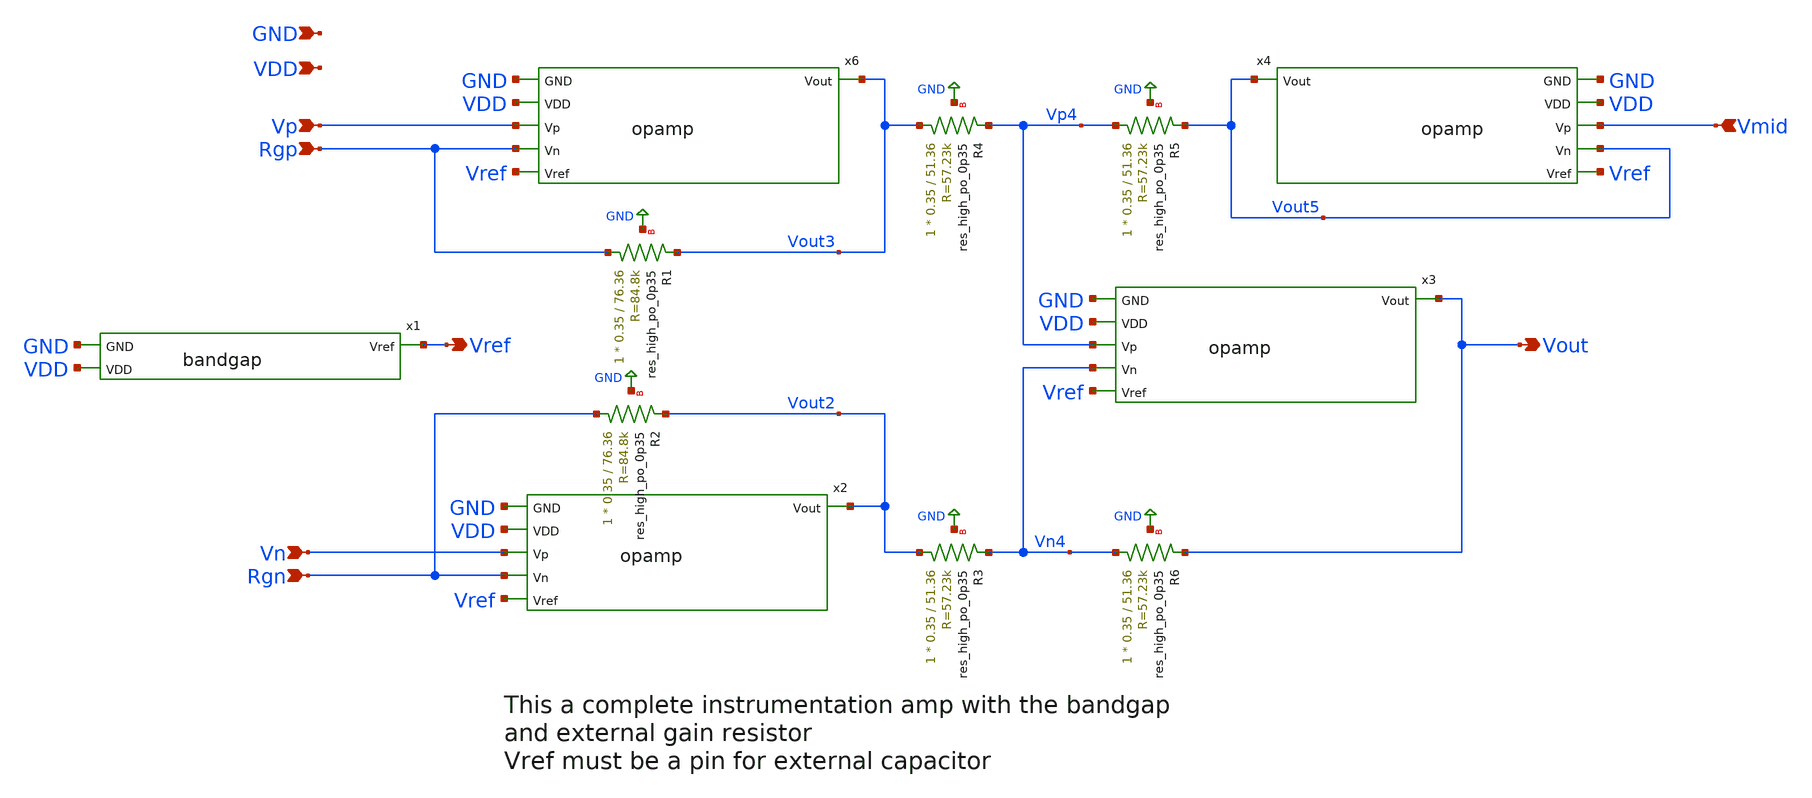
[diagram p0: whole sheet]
** sch_path: xschem/instamp.sch
* Copyright 2021 Stefan Frederik Schippers
* Licensed under the Apache License, Version 2.0 (the "License");
* you may not use this file except in compliance with the License.
* You may obtain a copy of the License at
* https://www.apache.org/licenses/LICENSE-2.0
* Unless required by applicable law or agreed to in writing, software
* distributed under the License is distributed on an "AS IS" BASIS,
* WITHOUT WARRANTIES OR CONDITIONS OF ANY KIND, either express or implied.
* See the License for the specific language governing permissions and
* limitations under the License.
**.subckt instamp Vp Vn Vout Vref Rgp Rgn Vmid GND VDD
*.ipin Vp
*.ipin Vn
*.opin Vout
*.opin Vref
*.ipin Rgp
*.ipin Rgn
*.ipin Vmid
*.ipin GND
*.ipin VDD
XR1 Rgp Vout3 GND sky130_fd_pr__res_high_po_0p35 L=76.36 mult=1 m=1
XR2 Rgn Vout2 GND sky130_fd_pr__res_high_po_0p35 L=76.36 mult=1 m=1
XR3 Vout2 Vn4 GND sky130_fd_pr__res_high_po_0p35 L=51.36 mult=1 m=1
XR4 Vout3 Vp4 GND sky130_fd_pr__res_high_po_0p35 L=51.36 mult=1 m=1
XR5 Vp4 Vout5 GND sky130_fd_pr__res_high_po_0p35 L=51.36 mult=1 m=1
XR6 Vn4 Vout GND sky130_fd_pr__res_high_po_0p35 L=51.36 mult=1 m=1
x6 Vref Vout3 Vp Rgp VDD GND opamp
x2 Vref Vout2 Vn Rgn VDD GND opamp
x3 Vref Vout Vp4 Vn4 VDD GND opamp
x4 Vref Vout5 Vmid Vout5 VDD GND opamp
x1 Vref GND VDD bandgap
**.ends

* expanding   symbol:  opamp.sym # of pins=6
** sym_path: xschem/opamp.sym
** sch_path: xschem/opamp.sch
.subckt opamp Vref Vout Vp Vn VDD GND
*.opin Vout
*.ipin Vref
*.ipin Vp
*.ipin Vn
*.ipin GND
*.ipin VDD
XM1 Vg1 Vg1 net1 GND sky130_fd_pr__nfet_g5v0d10v5 L=2 W=3.33 nf=1 ad='int((1 + 1)/2) * 3.33 / 1 * 0.29'
+ as='int((1 + 2)/2) * 3.33 / 1 * 0.29' pd='2*int((1 + 1)/2) * (3.33 / 1 + 0.29)' ps='2*int((1 + 2)/2) * (3.33 / 1 + 0.29)'
+ nrd='0.29 / 3.33 ' nrs='0.29 / 3.33 ' sa=0 sb=0 sd=0 mult=3 m=3
XM2 net1 Vg1 GND GND sky130_fd_pr__nfet_g5v0d10v5 L=5 W=5 nf=1 ad='int((1 + 1)/2) * 5 / 1 * 0.29' as='int((1 + 2)/2) * 5 / 1 * 0.29'
+ pd='2*int((1 + 1)/2) * (5 / 1 + 0.29)' ps='2*int((1 + 2)/2) * (5 / 1 + 0.29)' nrd='0.29 / 5 ' nrs='0.29 / 5 '
+ sa=0 sb=0 sd=0 mult=1 m=1
XM4 net2 Vg1 GND GND sky130_fd_pr__nfet_g5v0d10v5 L=5 W=5 nf=1 ad='int((1 + 1)/2) * 5 / 1 * 0.29' as='int((1 + 2)/2) * 5 / 1 * 0.29'
+ pd='2*int((1 + 1)/2) * (5 / 1 + 0.29)' ps='2*int((1 + 2)/2) * (5 / 1 + 0.29)' nrd='0.29 / 5 ' nrs='0.29 / 5 '
+ sa=0 sb=0 sd=0 mult=1 m=1
XM3 Vg5 Vg1 net2 GND sky130_fd_pr__nfet_g5v0d10v5 L=2 W=3.33 nf=1 ad='int((1 + 1)/2) * 3.33 / 1 * 0.29'
+ as='int((1 + 2)/2) * 3.33 / 1 * 0.29' pd='2*int((1 + 1)/2) * (3.33 / 1 + 0.29)' ps='2*int((1 + 2)/2) * (3.33 / 1 + 0.29)'
+ nrd='0.29 / 3.33 ' nrs='0.29 / 3.33 ' sa=0 sb=0 sd=0 mult=3 m=3
XMr1 net6 Vref GND GND sky130_fd_pr__nfet_g5v0d10v5 L=8 W=5 nf=1 ad='int((1 + 1)/2) * 5 / 1 * 0.29' as='int((1 + 2)/2) * 5 / 1 * 0.29'
+ pd='2*int((1 + 1)/2) * (5 / 1 + 0.29)' ps='2*int((1 + 2)/2) * (5 / 1 + 0.29)' nrd='0.29 / 5 ' nrs='0.29 / 5 '
+ sa=0 sb=0 sd=0 mult=1 m=1
XMr2 VgR2 VgR2 VDD VDD sky130_fd_pr__pfet_g5v0d10v5 L=5 W=4 nf=1 ad='int((1 + 1)/2) * 4 / 1 * 0.29' as='int((1 + 2)/2) * 4 / 1 * 0.29'
+ pd='2*int((1 + 1)/2) * (4 / 1 + 0.29)' ps='2*int((1 + 2)/2) * (4 / 1 + 0.29)' nrd='0.29 / 4 ' nrs='0.29 / 4 '
+ sa=0 sb=0 sd=0 mult=1 m=1
XMr3 Vg1 VgR2 VDD VDD sky130_fd_pr__pfet_g5v0d10v5 L=5 W=4 nf=1 ad='int((1 + 1)/2) * 4 / 1 * 0.29' as='int((1 + 2)/2) * 4 / 1 * 0.29'
+ pd='2*int((1 + 1)/2) * (4 / 1 + 0.29)' ps='2*int((1 + 2)/2) * (4 / 1 + 0.29)' nrd='0.29 / 4 ' nrs='0.29 / 4 '
+ sa=0 sb=0 sd=0 mult=1 m=1
XM32 net3 Vg1 GND GND sky130_fd_pr__nfet_g5v0d10v5 L=5 W=10 nf=1 ad='int((1 + 1)/2) * 10 / 1 * 0.29'
+ as='int((1 + 2)/2) * 10 / 1 * 0.29' pd='2*int((1 + 1)/2) * (10 / 1 + 0.29)' ps='2*int((1 + 2)/2) * (10 / 1 + 0.29)'
+ nrd='0.29 / 10 ' nrs='0.29 / 10 ' sa=0 sb=0 sd=0 mult=1 m=1
XM31 Vs29 Vg1 net3 GND sky130_fd_pr__nfet_g5v0d10v5 L=2 W=6.66 nf=1 ad='int((1 + 1)/2) * 6.66 / 1 * 0.29'
+ as='int((1 + 2)/2) * 6.66 / 1 * 0.29' pd='2*int((1 + 1)/2) * (6.66 / 1 + 0.29)' ps='2*int((1 + 2)/2) * (6.66 / 1 + 0.29)'
+ nrd='0.29 / 6.66 ' nrs='0.29 / 6.66 ' sa=0 sb=0 sd=0 mult=3 m=3
XM15 Vg11 Vg1 Vd10 GND sky130_fd_pr__nfet_g5v0d10v5 L=2 W=14.3 nf=1 ad='int((1 + 1)/2) * 14.3 / 1 * 0.29'
+ as='int((1 + 2)/2) * 14.3 / 1 * 0.29' pd='2*int((1 + 1)/2) * (14.3 / 1 + 0.29)' ps='2*int((1 + 2)/2) * (14.3 / 1 + 0.29)'
+ nrd='0.29 / 14.3 ' nrs='0.29 / 14.3 ' sa=0 sb=0 sd=0 mult=7 m=7
XM16 Vd10 Vg1 GND GND sky130_fd_pr__nfet_g5v0d10v5 L=5 W=10 nf=1 ad='int((1 + 1)/2) * 10 / 1 * 0.29'
+ as='int((1 + 2)/2) * 10 / 1 * 0.29' pd='2*int((1 + 1)/2) * (10 / 1 + 0.29)' ps='2*int((1 + 2)/2) * (10 / 1 + 0.29)'
+ nrd='0.29 / 10 ' nrs='0.29 / 10 ' sa=0 sb=0 sd=0 mult=1 m=1
XM18 Vd9 Vg1 GND GND sky130_fd_pr__nfet_g5v0d10v5 L=5 W=10 nf=1 ad='int((1 + 1)/2) * 10 / 1 * 0.29' as='int((1 + 2)/2) * 10 / 1 * 0.29'
+ pd='2*int((1 + 1)/2) * (10 / 1 + 0.29)' ps='2*int((1 + 2)/2) * (10 / 1 + 0.29)' nrd='0.29 / 10 ' nrs='0.29 / 10 '
+ sa=0 sb=0 sd=0 mult=1 m=1
XM17 Vg28 Vg1 Vd9 GND sky130_fd_pr__nfet_g5v0d10v5 L=2 W=14.3 nf=1 ad='int((1 + 1)/2) * 14.3 / 1 * 0.29'
+ as='int((1 + 2)/2) * 14.3 / 1 * 0.29' pd='2*int((1 + 1)/2) * (14.3 / 1 + 0.29)' ps='2*int((1 + 2)/2) * (14.3 / 1 + 0.29)'
+ nrd='0.29 / 14.3 ' nrs='0.29 / 14.3 ' sa=0 sb=0 sd=0 mult=7 m=7
XM20 Vg22 Vg1 GND GND sky130_fd_pr__nfet_g5v0d10v5 L=5 W=1.5 nf=1 ad='int((1 + 1)/2) * 1.5 / 1 * 0.29'
+ as='int((1 + 2)/2) * 1.5 / 1 * 0.29' pd='2*int((1 + 1)/2) * (1.5 / 1 + 0.29)' ps='2*int((1 + 2)/2) * (1.5 / 1 + 0.29)'
+ nrd='0.29 / 1.5 ' nrs='0.29 / 1.5 ' sa=0 sb=0 sd=0 mult=1 m=1
XM26 Vg26 Vg26 GND GND sky130_fd_pr__nfet_g5v0d10v5 L=0.5 W=5 nf=1 ad='int((1 + 1)/2) * 5 / 1 * 0.29'
+ as='int((1 + 2)/2) * 5 / 1 * 0.29' pd='2*int((1 + 1)/2) * (5 / 1 + 0.29)' ps='2*int((1 + 2)/2) * (5 / 1 + 0.29)'
+ nrd='0.29 / 5 ' nrs='0.29 / 5 ' sa=0 sb=0 sd=0 mult=5 m=5
XM25 Vd24 Vd24 Vg26 GND sky130_fd_pr__nfet_g5v0d10v5 L=0.5 W=5 nf=1 ad='int((1 + 1)/2) * 5 / 1 * 0.29'
+ as='int((1 + 2)/2) * 5 / 1 * 0.29' pd='2*int((1 + 1)/2) * (5 / 1 + 0.29)' ps='2*int((1 + 2)/2) * (5 / 1 + 0.29)'
+ nrd='0.29 / 5 ' nrs='0.29 / 5 ' sa=0 sb=0 sd=0 mult=5 m=5
XM23 Vg27 Vd24 Vg28 GND sky130_fd_pr__nfet_g5v0d10v5 L=0.5 W=10 nf=1 ad='int((1 + 1)/2) * 10 / 1 * 0.29'
+ as='int((1 + 2)/2) * 10 / 1 * 0.29' pd='2*int((1 + 1)/2) * (10 / 1 + 0.29)' ps='2*int((1 + 2)/2) * (10 / 1 + 0.29)'
+ nrd='0.29 / 10 ' nrs='0.29 / 10 ' sa=0 sb=0 sd=0 mult=5 m=5
XM28 Vout Vg28 GND GND sky130_fd_pr__nfet_g5v0d10v5 L=0.5 W=10 nf=1 ad='int((1 + 1)/2) * 10 / 1 * 0.29'
+ as='int((1 + 2)/2) * 10 / 1 * 0.29' pd='2*int((1 + 1)/2) * (10 / 1 + 0.29)' ps='2*int((1 + 2)/2) * (10 / 1 + 0.29)'
+ nrd='0.29 / 10 ' nrs='0.29 / 10 ' sa=0 sb=0 sd=0 mult=15 m=15
XM30 Vd30 Vn Vs29 GND sky130_fd_pr__nfet_g5v0d10v5 L=1.5 W=11.11 nf=1 ad='int((1 + 1)/2) * 11.11 / 1 * 0.29'
+ as='int((1 + 2)/2) * 11.11 / 1 * 0.29' pd='2*int((1 + 1)/2) * (11.11 / 1 + 0.29)' ps='2*int((1 + 2)/2) * (11.11 / 1 + 0.29)'
+ nrd='0.29 / 11.11 ' nrs='0.29 / 11.11 ' sa=0 sb=0 sd=0 mult=9 m=9
XM29 Vd29 Vp Vs29 GND sky130_fd_pr__nfet_g5v0d10v5 L=1.5 W=11.11 nf=1 ad='int((1 + 1)/2) * 11.11 / 1 * 0.29'
+ as='int((1 + 2)/2) * 11.11 / 1 * 0.29' pd='2*int((1 + 1)/2) * (11.11 / 1 + 0.29)' ps='2*int((1 + 2)/2) * (11.11 / 1 + 0.29)'
+ nrd='0.29 / 11.11 ' nrs='0.29 / 11.11 ' sa=0 sb=0 sd=0 mult=9 m=9
XM5 net4 Vg5 VDD VDD sky130_fd_pr__pfet_g5v0d10v5 L=5 W=5 nf=1 ad='int((1 + 1)/2) * 5 / 1 * 0.29' as='int((1 + 2)/2) * 5 / 1 * 0.29'
+ pd='2*int((1 + 1)/2) * (5 / 1 + 0.29)' ps='2*int((1 + 2)/2) * (5 / 1 + 0.29)' nrd='0.29 / 5 ' nrs='0.29 / 5 '
+ sa=0 sb=0 sd=0 mult=3 m=3
XM6 Vg5 Vg5 net4 VDD sky130_fd_pr__pfet_g5v0d10v5 L=2 W=6.6 nf=1 ad='int((1 + 1)/2) * 6.6 / 1 * 0.29'
+ as='int((1 + 2)/2) * 6.6 / 1 * 0.29' pd='2*int((1 + 1)/2) * (6.6 / 1 + 0.29)' ps='2*int((1 + 2)/2) * (6.6 / 1 + 0.29)'
+ nrd='0.29 / 6.6 ' nrs='0.29 / 6.6 ' sa=0 sb=0 sd=0 mult=3 m=3
XM7 net5 Vg5 VDD VDD sky130_fd_pr__pfet_g5v0d10v5 L=5 W=10 nf=1 ad='int((1 + 1)/2) * 10 / 1 * 0.29' as='int((1 + 2)/2) * 10 / 1 * 0.29'
+ pd='2*int((1 + 1)/2) * (10 / 1 + 0.29)' ps='2*int((1 + 2)/2) * (10 / 1 + 0.29)' nrd='0.29 / 10 ' nrs='0.29 / 10 '
+ sa=0 sb=0 sd=0 mult=3 m=3
XM8 Vd8 Vg5 net5 VDD sky130_fd_pr__pfet_g5v0d10v5 L=2 W=13.2 nf=1 ad='int((1 + 1)/2) * 13.2 / 1 * 0.29'
+ as='int((1 + 2)/2) * 13.2 / 1 * 0.29' pd='2*int((1 + 1)/2) * (13.2 / 1 + 0.29)' ps='2*int((1 + 2)/2) * (13.2 / 1 + 0.29)'
+ nrd='0.29 / 13.2 ' nrs='0.29 / 13.2 ' sa=0 sb=0 sd=0 mult=3 m=3
XM09 Vd9 Vp Vd8 Vd8 sky130_fd_pr__pfet_g5v0d10v5 L=1.5 W=22.22 nf=1 ad='int((1 + 1)/2) * 22.22 / 1 * 0.29'
+ as='int((1 + 2)/2) * 22.22 / 1 * 0.29' pd='2*int((1 + 1)/2) * (22.22 / 1 + 0.29)' ps='2*int((1 + 2)/2) * (22.22 / 1 + 0.29)'
+ nrd='0.29 / 22.22 ' nrs='0.29 / 22.22 ' sa=0 sb=0 sd=0 mult=9 m=9
XM010 Vd10 Vn Vd8 Vd8 sky130_fd_pr__pfet_g5v0d10v5 L=1.5 W=22.22 nf=1 ad='int((1 + 1)/2) * 22.22 / 1 * 0.29'
+ as='int((1 + 2)/2) * 22.22 / 1 * 0.29' pd='2*int((1 + 1)/2) * (22.22 / 1 + 0.29)' ps='2*int((1 + 2)/2) * (22.22 / 1 + 0.29)'
+ nrd='0.29 / 22.22 ' nrs='0.29 / 22.22 ' sa=0 sb=0 sd=0 mult=9 m=9
XM13 Vd29 Vg11 VDD VDD sky130_fd_pr__pfet_g5v0d10v5 L=2.5 W=10 nf=1 ad='int((1 + 1)/2) * 10 / 1 * 0.29'
+ as='int((1 + 2)/2) * 10 / 1 * 0.29' pd='2*int((1 + 1)/2) * (10 / 1 + 0.29)' ps='2*int((1 + 2)/2) * (10 / 1 + 0.29)'
+ nrd='0.29 / 10 ' nrs='0.29 / 10 ' sa=0 sb=0 sd=0 mult=5 m=5
XM14 Vg27 Vg11 Vd29 VDD sky130_fd_pr__pfet_g5v0d10v5 L=1 W=10 nf=1 ad='int((1 + 1)/2) * 10 / 1 * 0.29'
+ as='int((1 + 2)/2) * 10 / 1 * 0.29' pd='2*int((1 + 1)/2) * (10 / 1 + 0.29)' ps='2*int((1 + 2)/2) * (10 / 1 + 0.29)'
+ nrd='0.29 / 10 ' nrs='0.29 / 10 ' sa=0 sb=0 sd=0 mult=5 m=5
XM11 Vd30 Vg11 VDD VDD sky130_fd_pr__pfet_g5v0d10v5 L=2.5 W=10 nf=1 ad='int((1 + 1)/2) * 10 / 1 * 0.29'
+ as='int((1 + 2)/2) * 10 / 1 * 0.29' pd='2*int((1 + 1)/2) * (10 / 1 + 0.29)' ps='2*int((1 + 2)/2) * (10 / 1 + 0.29)'
+ nrd='0.29 / 10 ' nrs='0.29 / 10 ' sa=0 sb=0 sd=0 mult=5 m=5
XM12 Vg11 Vg11 Vd30 VDD sky130_fd_pr__pfet_g5v0d10v5 L=1 W=10 nf=1 ad='int((1 + 1)/2) * 10 / 1 * 0.29'
+ as='int((1 + 2)/2) * 10 / 1 * 0.29' pd='2*int((1 + 1)/2) * (10 / 1 + 0.29)' ps='2*int((1 + 2)/2) * (10 / 1 + 0.29)'
+ nrd='0.29 / 10 ' nrs='0.29 / 10 ' sa=0 sb=0 sd=0 mult=5 m=5
XM021 Vg21 Vg21 VDD VDD sky130_fd_pr__pfet_g5v0d10v5 L=0.5 W=15 nf=1 ad='int((1 + 1)/2) * 15 / 1 * 0.29'
+ as='int((1 + 2)/2) * 15 / 1 * 0.29' pd='2*int((1 + 1)/2) * (15 / 1 + 0.29)' ps='2*int((1 + 2)/2) * (15 / 1 + 0.29)'
+ nrd='0.29 / 15 ' nrs='0.29 / 15 ' sa=0 sb=0 sd=0 mult=5 m=5
XM022 Vg22 Vg22 Vg21 VDD sky130_fd_pr__pfet_g5v0d10v5 L=0.5 W=15 nf=1 ad='int((1 + 1)/2) * 15 / 1 * 0.29'
+ as='int((1 + 2)/2) * 15 / 1 * 0.29' pd='2*int((1 + 1)/2) * (15 / 1 + 0.29)' ps='2*int((1 + 2)/2) * (15 / 1 + 0.29)'
+ nrd='0.29 / 15 ' nrs='0.29 / 15 ' sa=0 sb=0 sd=0 mult=5 m=5
XM24 Vd24 Vg5 VDD VDD sky130_fd_pr__pfet_g5v0d10v5 L=5 W=4 nf=1 ad='int((1 + 1)/2) * 4 / 1 * 0.29' as='int((1 + 2)/2) * 4 / 1 * 0.29'
+ pd='2*int((1 + 1)/2) * (4 / 1 + 0.29)' ps='2*int((1 + 2)/2) * (4 / 1 + 0.29)' nrd='0.29 / 4 ' nrs='0.29 / 4 '
+ sa=0 sb=0 sd=0 mult=1 m=1
XM27 Vout Vg27 VDD VDD sky130_fd_pr__pfet_g5v0d10v5 L=0.5 W=15 nf=1 ad='int((1 + 1)/2) * 15 / 1 * 0.29'
+ as='int((1 + 2)/2) * 15 / 1 * 0.29' pd='2*int((1 + 1)/2) * (15 / 1 + 0.29)' ps='2*int((1 + 2)/2) * (15 / 1 + 0.29)'
+ nrd='0.29 / 15 ' nrs='0.29 / 15 ' sa=0 sb=0 sd=0 mult=25 m=25
XM19 Vg28 Vg22 Vg27 VDD sky130_fd_pr__pfet_g5v0d10v5 L=0.5 W=10 nf=1 ad='int((1 + 1)/2) * 10 / 1 * 0.29'
+ as='int((1 + 2)/2) * 10 / 1 * 0.29' pd='2*int((1 + 1)/2) * (10 / 1 + 0.29)' ps='2*int((1 + 2)/2) * (10 / 1 + 0.29)'
+ nrd='0.29 / 10 ' nrs='0.29 / 10 ' sa=0 sb=0 sd=0 mult=15 m=15
Vmeas_Iref VgR2 net6 0
.save i(vmeas_iref)
XC1 Vg27 Vout sky130_fd_pr__cap_mim_m3_1 W=30 L=20 MF=4 m=4
XC2 Vg28 Vout sky130_fd_pr__cap_mim_m3_1 W=30 L=20 MF=4 m=4
.ends


* expanding   symbol:  bandgap.sym # of pins=3
** sym_path: xschem/bandgap.sym
** sch_path: xschem/bandgap.sch
.subckt bandgap Vref GND VDD
*.opin Vref
*.ipin GND
*.ipin VDD
XM4 Vg3 Vg3 GND GND sky130_fd_pr__nfet_g5v0d10v5 L=1 W=20 nf=1 ad='int((1 + 1)/2) * 20 / 1 * 0.29' as='int((1 + 2)/2) * 20 / 1 * 0.29'
+ pd='2*int((1 + 1)/2) * (20 / 1 + 0.29)' ps='2*int((1 + 2)/2) * (20 / 1 + 0.29)' nrd='0.29 / 20 ' nrs='0.29 / 20 '
+ sa=0 sb=0 sd=0 mult=1 m=1
XQ1 GND GND Ve1 sky130_fd_pr__pnp_05v5_W3p40L3p40 m=24
XQ2 GND GND Vg2 sky130_fd_pr__pnp_05v5_W3p40L3p40 m=1
XM1 Vg10 Vg1 net1 net1 sky130_fd_pr__pfet_g5v0d10v5 L=1 W=20 nf=1 ad='int((1 + 1)/2) * 20 / 1 * 0.29'
+ as='int((1 + 2)/2) * 20 / 1 * 0.29' pd='2*int((1 + 1)/2) * (20 / 1 + 0.29)' ps='2*int((1 + 2)/2) * (20 / 1 + 0.29)'
+ nrd='0.29 / 20 ' nrs='0.29 / 20 ' sa=0 sb=0 sd=0 mult=1 m=1
XM2 Vg3 Vg2 net1 net1 sky130_fd_pr__pfet_g5v0d10v5 L=1 W=20 nf=1 ad='int((1 + 1)/2) * 20 / 1 * 0.29'
+ as='int((1 + 2)/2) * 20 / 1 * 0.29' pd='2*int((1 + 1)/2) * (20 / 1 + 0.29)' ps='2*int((1 + 2)/2) * (20 / 1 + 0.29)'
+ nrd='0.29 / 20 ' nrs='0.29 / 20 ' sa=0 sb=0 sd=0 mult=1 m=1
XM11 net1 Vg5 VDD VDD sky130_fd_pr__pfet_g5v0d10v5 L=1 W=1 nf=1 ad='int((1 + 1)/2) * 1 / 1 * 0.29' as='int((1 + 2)/2) * 1 / 1 * 0.29'
+ pd='2*int((1 + 1)/2) * (1 / 1 + 0.29)' ps='2*int((1 + 2)/2) * (1 / 1 + 0.29)' nrd='0.29 / 1 ' nrs='0.29 / 1 '
+ sa=0 sb=0 sd=0 mult=1 m=1
XM3 Vg10 Vg3 GND GND sky130_fd_pr__nfet_g5v0d10v5 L=1 W=20 nf=1 ad='int((1 + 1)/2) * 20 / 1 * 0.29' as='int((1 + 2)/2) * 20 / 1 * 0.29'
+ pd='2*int((1 + 1)/2) * (20 / 1 + 0.29)' ps='2*int((1 + 2)/2) * (20 / 1 + 0.29)' nrd='0.29 / 20 ' nrs='0.29 / 20 '
+ sa=0 sb=0 sd=0 mult=1 m=1
XM10 net2 Vg10 GND GND sky130_fd_pr__nfet_g5v0d10v5 L=1 W=20 nf=1 ad='int((1 + 1)/2) * 20 / 1 * 0.29'
+ as='int((1 + 2)/2) * 20 / 1 * 0.29' pd='2*int((1 + 1)/2) * (20 / 1 + 0.29)' ps='2*int((1 + 2)/2) * (20 / 1 + 0.29)'
+ nrd='0.29 / 20 ' nrs='0.29 / 20 ' sa=0 sb=0 sd=0 mult=1 m=1
XM8 Vg12 Vg5 VDD VDD sky130_fd_pr__pfet_g5v0d10v5 L=1 W=1 nf=1 ad='int((1 + 1)/2) * 1 / 1 * 0.29' as='int((1 + 2)/2) * 1 / 1 * 0.29'
+ pd='2*int((1 + 1)/2) * (1 / 1 + 0.29)' ps='2*int((1 + 2)/2) * (1 / 1 + 0.29)' nrd='0.29 / 1 ' nrs='0.29 / 1 '
+ sa=0 sb=0 sd=0 mult=1 m=1
XM5 Vg5 Vg5 VDD VDD sky130_fd_pr__pfet_g5v0d10v5 L=1 W=1 nf=1 ad='int((1 + 1)/2) * 1 / 1 * 0.29' as='int((1 + 2)/2) * 1 / 1 * 0.29'
+ pd='2*int((1 + 1)/2) * (1 / 1 + 0.29)' ps='2*int((1 + 2)/2) * (1 / 1 + 0.29)' nrd='0.29 / 1 ' nrs='0.29 / 1 '
+ sa=0 sb=0 sd=0 mult=1 m=1
XM12 Vref Vg12 VDD VDD sky130_fd_pr__pfet_g5v0d10v5 L=0.5 W=20 nf=1 ad='int((1 + 1)/2) * 20 / 1 * 0.29'
+ as='int((1 + 2)/2) * 20 / 1 * 0.29' pd='2*int((1 + 1)/2) * (20 / 1 + 0.29)' ps='2*int((1 + 2)/2) * (20 / 1 + 0.29)'
+ nrd='0.29 / 20 ' nrs='0.29 / 20 ' sa=0 sb=0 sd=0 mult=1 m=1
XM9 Vg12 Vref net2 GND sky130_fd_pr__nfet_g5v0d10v5 L=1 W=20 nf=1 ad='int((1 + 1)/2) * 20 / 1 * 0.29'
+ as='int((1 + 2)/2) * 20 / 1 * 0.29' pd='2*int((1 + 1)/2) * (20 / 1 + 0.29)' ps='2*int((1 + 2)/2) * (20 / 1 + 0.29)'
+ nrd='0.29 / 20 ' nrs='0.29 / 20 ' sa=0 sb=0 sd=0 mult=1 m=1
XM7a Vg12 Vg12 net6 GND sky130_fd_pr__nfet_g5v0d10v5 L=10 W=0.5 nf=1 ad='int((1 + 1)/2) * 0.5 / 1 * 0.29'
+ as='int((1 + 2)/2) * 0.5 / 1 * 0.29' pd='2*int((1 + 1)/2) * (0.5 / 1 + 0.29)' ps='2*int((1 + 2)/2) * (0.5 / 1 + 0.29)'
+ nrd='0.29 / 0.5 ' nrs='0.29 / 0.5 ' sa=0 sb=0 sd=0 mult=1 m=1
XM7b net6 Vg12 net5 GND sky130_fd_pr__nfet_g5v0d10v5 L=10 W=0.5 nf=1 ad='int((1 + 1)/2) * 0.5 / 1 * 0.29'
+ as='int((1 + 2)/2) * 0.5 / 1 * 0.29' pd='2*int((1 + 1)/2) * (0.5 / 1 + 0.29)' ps='2*int((1 + 2)/2) * (0.5 / 1 + 0.29)'
+ nrd='0.29 / 0.5 ' nrs='0.29 / 0.5 ' sa=0 sb=0 sd=0 mult=1 m=1
XM7c net5 Vg12 net4 GND sky130_fd_pr__nfet_g5v0d10v5 L=10 W=0.5 nf=1 ad='int((1 + 1)/2) * 0.5 / 1 * 0.29'
+ as='int((1 + 2)/2) * 0.5 / 1 * 0.29' pd='2*int((1 + 1)/2) * (0.5 / 1 + 0.29)' ps='2*int((1 + 2)/2) * (0.5 / 1 + 0.29)'
+ nrd='0.29 / 0.5 ' nrs='0.29 / 0.5 ' sa=0 sb=0 sd=0 mult=1 m=1
XM7d net4 Vg12 net3 GND sky130_fd_pr__nfet_g5v0d10v5 L=10 W=0.5 nf=1 ad='int((1 + 1)/2) * 0.5 / 1 * 0.29'
+ as='int((1 + 2)/2) * 0.5 / 1 * 0.29' pd='2*int((1 + 1)/2) * (0.5 / 1 + 0.29)' ps='2*int((1 + 2)/2) * (0.5 / 1 + 0.29)'
+ nrd='0.29 / 0.5 ' nrs='0.29 / 0.5 ' sa=0 sb=0 sd=0 mult=1 m=1
XM7e net3 Vg12 net11 GND sky130_fd_pr__nfet_g5v0d10v5 L=10 W=0.5 nf=1 ad='int((1 + 1)/2) * 0.5 / 1 * 0.29'
+ as='int((1 + 2)/2) * 0.5 / 1 * 0.29' pd='2*int((1 + 1)/2) * (0.5 / 1 + 0.29)' ps='2*int((1 + 2)/2) * (0.5 / 1 + 0.29)'
+ nrd='0.29 / 0.5 ' nrs='0.29 / 0.5 ' sa=0 sb=0 sd=0 mult=1 m=1
XM6 Vg5 Vref Vs5 GND sky130_fd_pr__nfet_g5v0d10v5 L=1 W=5 nf=1 ad='int((1 + 1)/2) * 5 / 1 * 0.29' as='int((1 + 2)/2) * 5 / 1 * 0.29'
+ pd='2*int((1 + 1)/2) * (5 / 1 + 0.29)' ps='2*int((1 + 2)/2) * (5 / 1 + 0.29)' nrd='0.29 / 5 ' nrs='0.29 / 5 '
+ sa=0 sb=0 sd=0 mult=1 m=1
XR1 Vg2 Vref GND sky130_fd_pr__res_high_po_0p35 L=20.1 mult=1 m=1
XR2 Vg1 Vref GND sky130_fd_pr__res_high_po_0p35 L=20.1 mult=1 m=1
XR4 GND Vs5 GND sky130_fd_pr__res_high_po_0p35 L=49.12 mult=1 m=1
XM7f net11 Vg12 net10 GND sky130_fd_pr__nfet_g5v0d10v5 L=10 W=0.5 nf=1 ad='int((1 + 1)/2) * 0.5 / 1 * 0.29'
+ as='int((1 + 2)/2) * 0.5 / 1 * 0.29' pd='2*int((1 + 1)/2) * (0.5 / 1 + 0.29)' ps='2*int((1 + 2)/2) * (0.5 / 1 + 0.29)'
+ nrd='0.29 / 0.5 ' nrs='0.29 / 0.5 ' sa=0 sb=0 sd=0 mult=1 m=1
XM7g net10 Vg12 net9 GND sky130_fd_pr__nfet_g5v0d10v5 L=10 W=0.5 nf=1 ad='int((1 + 1)/2) * 0.5 / 1 * 0.29'
+ as='int((1 + 2)/2) * 0.5 / 1 * 0.29' pd='2*int((1 + 1)/2) * (0.5 / 1 + 0.29)' ps='2*int((1 + 2)/2) * (0.5 / 1 + 0.29)'
+ nrd='0.29 / 0.5 ' nrs='0.29 / 0.5 ' sa=0 sb=0 sd=0 mult=1 m=1
XM7h net9 Vg12 net8 GND sky130_fd_pr__nfet_g5v0d10v5 L=10 W=0.5 nf=1 ad='int((1 + 1)/2) * 0.5 / 1 * 0.29'
+ as='int((1 + 2)/2) * 0.5 / 1 * 0.29' pd='2*int((1 + 1)/2) * (0.5 / 1 + 0.29)' ps='2*int((1 + 2)/2) * (0.5 / 1 + 0.29)'
+ nrd='0.29 / 0.5 ' nrs='0.29 / 0.5 ' sa=0 sb=0 sd=0 mult=1 m=1
XM7I net8 Vg12 net7 GND sky130_fd_pr__nfet_g5v0d10v5 L=10 W=0.5 nf=1 ad='int((1 + 1)/2) * 0.5 / 1 * 0.29'
+ as='int((1 + 2)/2) * 0.5 / 1 * 0.29' pd='2*int((1 + 1)/2) * (0.5 / 1 + 0.29)' ps='2*int((1 + 2)/2) * (0.5 / 1 + 0.29)'
+ nrd='0.29 / 0.5 ' nrs='0.29 / 0.5 ' sa=0 sb=0 sd=0 mult=1 m=1
XM7J net7 Vg12 GND GND sky130_fd_pr__nfet_g5v0d10v5 L=10 W=0.5 nf=1 ad='int((1 + 1)/2) * 0.5 / 1 * 0.29'
+ as='int((1 + 2)/2) * 0.5 / 1 * 0.29' pd='2*int((1 + 1)/2) * (0.5 / 1 + 0.29)' ps='2*int((1 + 2)/2) * (0.5 / 1 + 0.29)'
+ nrd='0.29 / 0.5 ' nrs='0.29 / 0.5 ' sa=0 sb=0 sd=0 mult=1 m=1
XR3 Ve1 Vg1 GND sky130_fd_pr__res_high_po_0p69 L=6.99 mult=1 m=1
.ends

.GLOBAL GND
.GLOBAL VDD
.end
